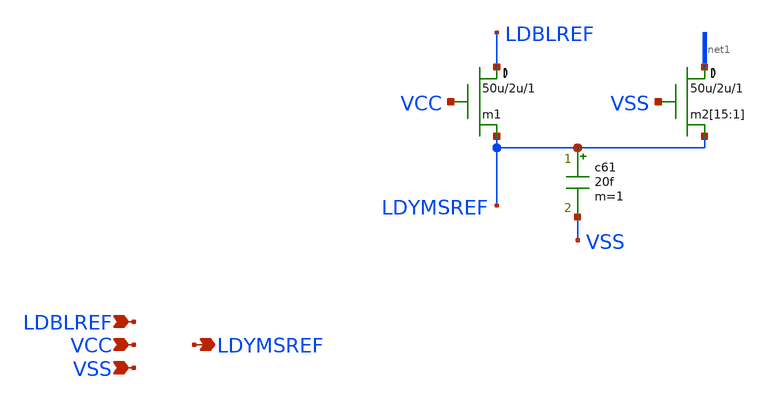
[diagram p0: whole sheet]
** sch_path: xschem_libs_newsym/rom8k/rom2_coldec_ref/schematic/rom2_coldec_ref.sch
* Copyright (C) 1998-2024 Stefan Frederik Schippers
* This program is free software; you can redistribute it and/or modify
* it under the terms of the GNU General Public License as published by
* the Free Software Foundation; either version 2 of the License, or
* (at your option) any later version.
* This program is distributed in the hope that it will be useful,
* but WITHOUT ANY WARRANTY; without even the implied warranty of
* MERCHANTABILITY or FITNESS FOR A PARTICULAR PURPOSE.  See the
* GNU General Public License for more details.
* You should have received a copy of the GNU General Public License
* along with this program; if not, write to the Free Software
**.subckt rom2_coldec_ref LDYMSREF LDBLREF VCC VSS
*.opin LDYMSREF
*.ipin LDBLREF
*.ipin VCC
*.ipin VSS
m1 LDBLREF VCC LDYMSREF 0 cmosn w=50u l=2u ad={50u *4.4u} as={50u *4.4u} pd={50u *2 + 8.8u} ps={50u *2 + 8.8u}
+ m=1
c61 LDYMSREF VSS 20f m=1
m2[15] net1[14] VSS LDYMSREF 0 cmosn w=50u l=2u ad={50u *4.4u} as={50u *4.4u} pd={50u *2 + 8.8u} ps={50u *2 + 8.8u}
+ m=1
m2[14] net1[13] VSS LDYMSREF 0 cmosn w=50u l=2u ad={50u *4.4u} as={50u *4.4u} pd={50u *2 + 8.8u} ps={50u *2 + 8.8u}
+ m=1
m2[13] net1[12] VSS LDYMSREF 0 cmosn w=50u l=2u ad={50u *4.4u} as={50u *4.4u} pd={50u *2 + 8.8u} ps={50u *2 + 8.8u}
+ m=1
m2[12] net1[11] VSS LDYMSREF 0 cmosn w=50u l=2u ad={50u *4.4u} as={50u *4.4u} pd={50u *2 + 8.8u} ps={50u *2 + 8.8u}
+ m=1
m2[11] net1[10] VSS LDYMSREF 0 cmosn w=50u l=2u ad={50u *4.4u} as={50u *4.4u} pd={50u *2 + 8.8u} ps={50u *2 + 8.8u}
+ m=1
m2[10] net1[9] VSS LDYMSREF 0 cmosn w=50u l=2u ad={50u *4.4u} as={50u *4.4u} pd={50u *2 + 8.8u} ps={50u *2 + 8.8u}
+ m=1
m2[9] net1[8] VSS LDYMSREF 0 cmosn w=50u l=2u ad={50u *4.4u} as={50u *4.4u} pd={50u *2 + 8.8u} ps={50u *2 + 8.8u}
+ m=1
m2[8] net1[7] VSS LDYMSREF 0 cmosn w=50u l=2u ad={50u *4.4u} as={50u *4.4u} pd={50u *2 + 8.8u} ps={50u *2 + 8.8u}
+ m=1
m2[7] net1[6] VSS LDYMSREF 0 cmosn w=50u l=2u ad={50u *4.4u} as={50u *4.4u} pd={50u *2 + 8.8u} ps={50u *2 + 8.8u}
+ m=1
m2[6] net1[5] VSS LDYMSREF 0 cmosn w=50u l=2u ad={50u *4.4u} as={50u *4.4u} pd={50u *2 + 8.8u} ps={50u *2 + 8.8u}
+ m=1
m2[5] net1[4] VSS LDYMSREF 0 cmosn w=50u l=2u ad={50u *4.4u} as={50u *4.4u} pd={50u *2 + 8.8u} ps={50u *2 + 8.8u}
+ m=1
m2[4] net1[3] VSS LDYMSREF 0 cmosn w=50u l=2u ad={50u *4.4u} as={50u *4.4u} pd={50u *2 + 8.8u} ps={50u *2 + 8.8u}
+ m=1
m2[3] net1[2] VSS LDYMSREF 0 cmosn w=50u l=2u ad={50u *4.4u} as={50u *4.4u} pd={50u *2 + 8.8u} ps={50u *2 + 8.8u}
+ m=1
m2[2] net1[1] VSS LDYMSREF 0 cmosn w=50u l=2u ad={50u *4.4u} as={50u *4.4u} pd={50u *2 + 8.8u} ps={50u *2 + 8.8u}
+ m=1
m2[1] net1[0] VSS LDYMSREF 0 cmosn w=50u l=2u ad={50u *4.4u} as={50u *4.4u} pd={50u *2 + 8.8u} ps={50u *2 + 8.8u}
+ m=1
**.ends
.end
